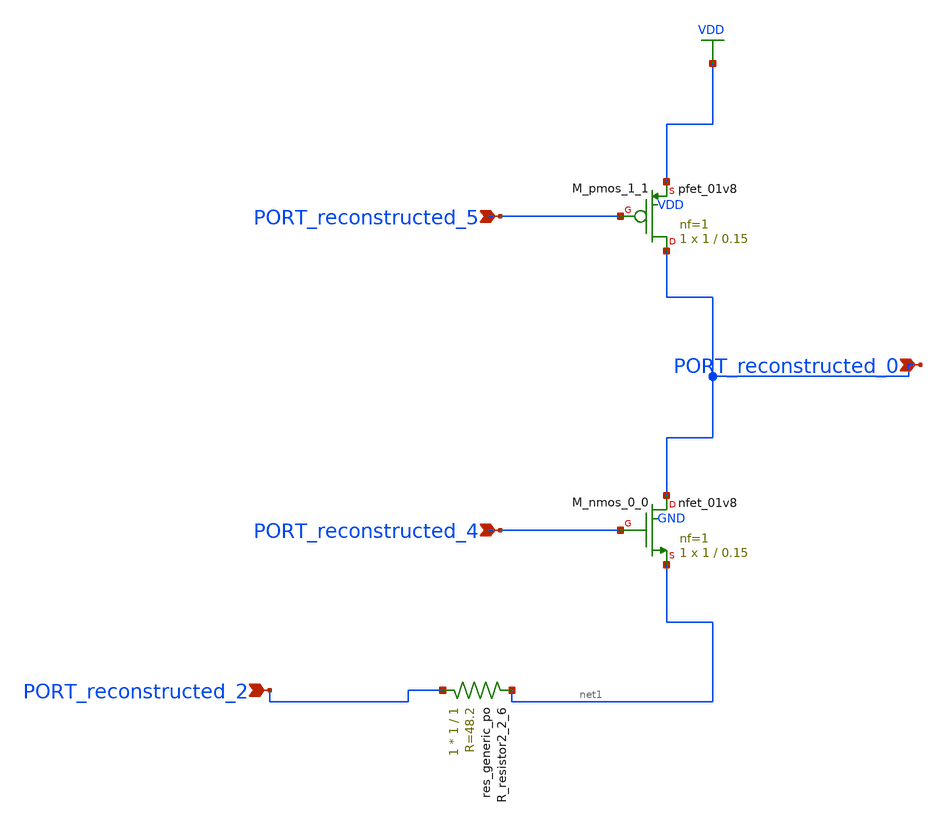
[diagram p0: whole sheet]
** sch_path: schematics/AMSNet/154.sch
**.subckt 154 PORT_reconstructed_5 PORT_reconstructed_4 PORT_reconstructed_0 PORT_reconstructed_2
*.ipin PORT_reconstructed_5
*.ipin PORT_reconstructed_4
*.ipin PORT_reconstructed_0
*.ipin PORT_reconstructed_2
XM_nmos_0_0 PORT_reconstructed_0 PORT_reconstructed_4 net1 GND sky130_fd_pr__nfet_01v8 L=0.15 W=1 nf=1
+ ad='int((1 + 1)/2) * 1 / 1 * 0.29' as='int((1 + 2)/2) * 1 / 1 * 0.29' pd='2*int((1 + 1)/2) * (1 / 1 + 0.29)'
+ ps='2*int((1 + 2)/2) * (1 / 1 + 0.29)' nrd='0.29 / 1 ' nrs='0.29 / 1 ' sa=0 sb=0 sd=0 mult=1 m=1
XM_pmos_1_1 PORT_reconstructed_0 PORT_reconstructed_5 VDD VDD sky130_fd_pr__pfet_01v8 L=0.15 W=1 nf=1
+ ad='int((1 + 1)/2) * 1 / 1 * 0.29' as='int((1 + 2)/2) * 1 / 1 * 0.29' pd='2*int((1 + 1)/2) * (1 / 1 + 0.29)'
+ ps='2*int((1 + 2)/2) * (1 / 1 + 0.29)' nrd='0.29 / 1 ' nrs='0.29 / 1 ' sa=0 sb=0 sd=0 mult=1 m=1
XR_resistor2_2_6 PORT_reconstructed_2 net1 sky130_fd_pr__res_generic_po W=1 L=1 m=1
**.ends
.GLOBAL VDD
.end
